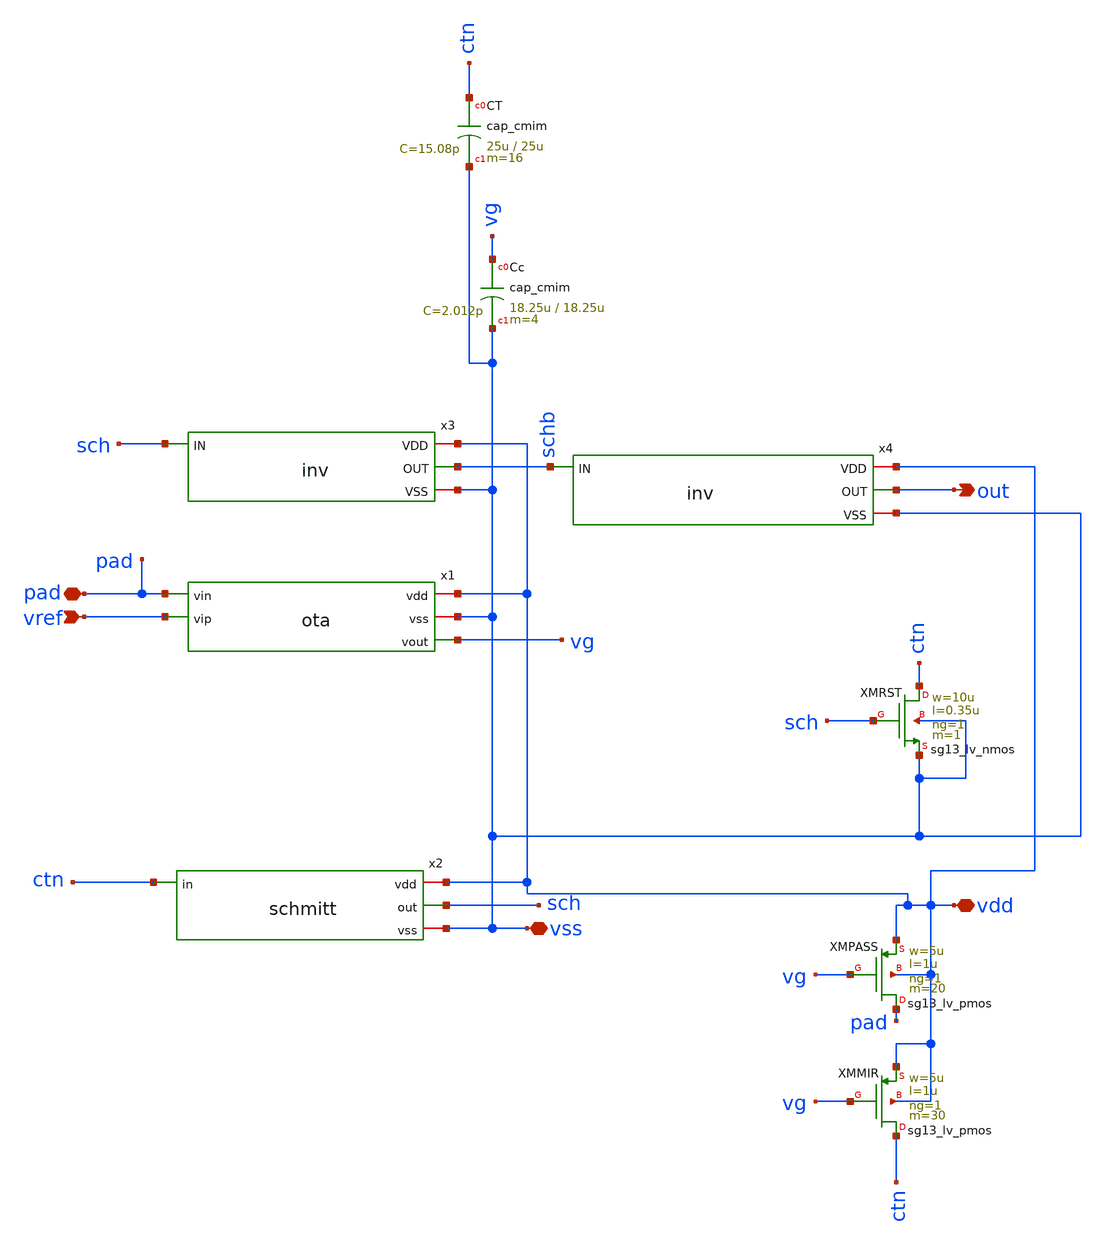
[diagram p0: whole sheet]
** sch_path: macros/heichips26_chronosense/schematic/xschem/chronosense_core.sch
* macros/heichips26_chronosense/schematic/xschem/inv.sch:
* Copyright 2023 IHP PDK Authors
* Licensed under the Apache License, Version 2.0 (the "License");
**.subckt chronosense_core pad vref out vss vdd
*.iopin pad
*.ipin vref
*.opin out
*.iopin vss
*.iopin vdd
x1 vdd pad vref vss vg ota
x3 vdd sch schb vss inv
x4 vdd schb out vss inv
XXMRST ctn sch vss vss sg13_lv_nmos w=10u l=0.35u ng=1 m=1 mm_ok=1
XXMPASS pad vg vdd vdd sg13_lv_pmos w=5u l=1u ng=1 m=20 mm_ok=1
XXMMIR ctn vg vdd vdd sg13_lv_pmos w=5u l=1u ng=1 m=30 mm_ok=1
XCc vg vss cap_cmim w=18.25u l=18.25u m=4 mm_ok=1
XCT ctn vss cap_cmim w=25u l=25u m=16 mm_ok=1
x2 vdd sch ctn vss schmitt
**.ends

* expanding   symbol:  ota.sym # of pins=5
** sym_path: macros/heichips26_chronosense/schematic/xschem/ota.sym
** sch_path: macros/heichips26_chronosense/schematic/xschem/ota.sch
.subckt ota vdd vin vip vss vout
*.opin vout
*.ipin vin
*.ipin vip
*.iopin vdd
*.iopin vss
XM1 vx vin vtail vss sg13_lv_nmos w=5u l=0.5u ng=1 m=4 mm_ok=1
XM3 vx vx vdd vdd sg13_lv_pmos w=5u l=1u ng=1 m=2 mm_ok=1
XM2 vout vip vtail vss sg13_lv_nmos w=5u l=0.5u ng=1 m=4 mm_ok=1
XM6 vb vb vss vss sg13_lv_nmos w=5u l=1u ng=1 m=2 mm_ok=1
XM5 vtail vb vss vss sg13_lv_nmos w=5u l=1u ng=1 m=2 mm_ok=1
XM4 vout vx vdd vdd sg13_lv_pmos w=5u l=1u ng=1 m=2 mm_ok=1
XR2 vdd vb sub! rppd w=1u l=115.79u m=1 b=0 mm_ok=1
.ends


* expanding   symbol:  inv.sym # of pins=4
** sym_path: macros/heichips26_chronosense/schematic/xschem/inv.sym
** sch_path: macros/heichips26_chronosense/schematic/xschem/inv.sch
.subckt inv VDD IN OUT VSS
*.ipin in
*.opin out
*.iopin vdd
*.iopin vss
XM1 out in vdd vdd sg13_lv_pmos w=2u l=0.35u ng=1 m=1 mm_ok=1
XM2 out in vss vss sg13_lv_nmos w=1u l=0.35u ng=1 m=1 mm_ok=1
.ends


* expanding   symbol:  schmitt.sym # of pins=4
** sym_path: macros/heichips26_chronosense/schematic/xschem/schmitt.sym
** sch_path: macros/heichips26_chronosense/schematic/xschem/schmitt.sch
.subckt schmitt vdd out in vss
*.ipin in
*.iopin vdd
*.iopin vss
*.opin out
XM1 x in vss vss sg13_lv_nmos w=3u l=0.35u ng=1 m=1 mm_ok=1
XM2 y in vdd vdd sg13_lv_pmos w=6u l=0.35u ng=1 m=1 mm_ok=1
XM3 net1 in x vss sg13_lv_nmos w=3u l=0.35u ng=1 m=1 mm_ok=1
XM4 x net1 vdd vss sg13_lv_nmos w=3u l=0.35u ng=1 m=1 mm_ok=1
XM5 net1 in y vdd sg13_lv_pmos w=6u l=0.35u ng=1 m=1 mm_ok=1
XM6 y net1 vss vdd sg13_lv_pmos w=6u l=0.35u ng=1 m=1 mm_ok=1
x1 vdd net1 out vss inv
.ends

.end
